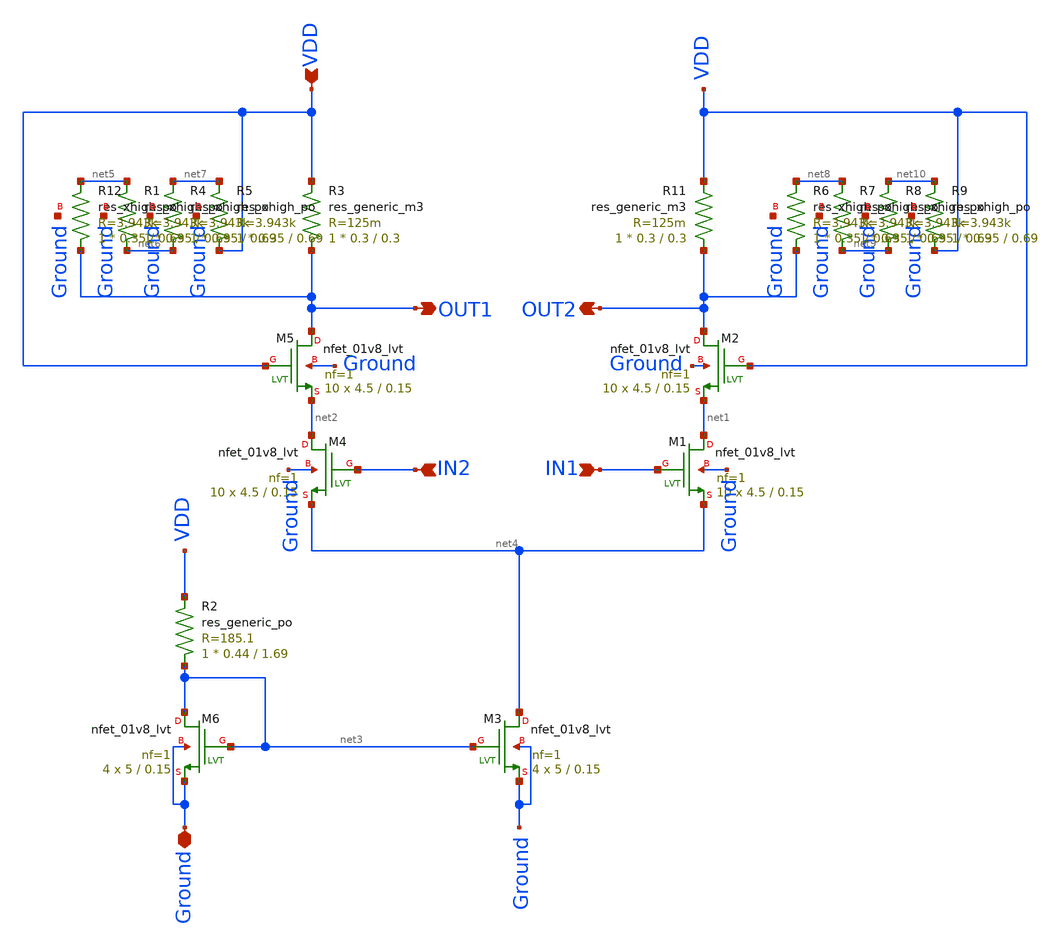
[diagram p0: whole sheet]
** sch_path: skywater_stuff/ECE631_RF_CMOS/Diff_LNA_LVS_1.sch
**.subckt Diff_LNA_LVS_1 IN1 IN2 VDD OUT1 OUT2 Ground
*.ipin IN1
*.ipin IN2
*.ipin VDD
*.opin OUT1
*.opin OUT2
*.iopin Ground
XM5 OUT1 VDD net2 Ground sky130_fd_pr__nfet_01v8_lvt L=0.15 W=4.5 nf=1 ad='int((nf+1)/2) * W/nf * 0.29'
+ as='int((nf+2)/2) * W/nf * 0.29' pd='2*int((nf+1)/2) * (W/nf + 0.29)' ps='2*int((nf+2)/2) * (W/nf + 0.29)'
+ nrd='0.29 / W' nrs='0.29 / W' sa=0 sb=0 sd=0 mult=10 m=10
XM3 net4 net3 Ground Ground sky130_fd_pr__nfet_01v8_lvt L=0.15 W=5 nf=1 ad='int((nf+1)/2) * W/nf * 0.29'
+ as='int((nf+2)/2) * W/nf * 0.29' pd='2*int((nf+1)/2) * (W/nf + 0.29)' ps='2*int((nf+2)/2) * (W/nf + 0.29)'
+ nrd='0.29 / W' nrs='0.29 / W' sa=0 sb=0 sd=0 mult=4 m=4
XM6 net3 net3 Ground Ground sky130_fd_pr__nfet_01v8_lvt L=0.15 W=5 nf=1 ad='int((nf+1)/2) * W/nf * 0.29'
+ as='int((nf+2)/2) * W/nf * 0.29' pd='2*int((nf+1)/2) * (W/nf + 0.29)' ps='2*int((nf+2)/2) * (W/nf + 0.29)'
+ nrd='0.29 / W' nrs='0.29 / W' sa=0 sb=0 sd=0 mult=4 m=4
XM4 net2 IN2 net4 Ground sky130_fd_pr__nfet_01v8_lvt L=0.15 W=4.5 nf=1 ad='int((nf+1)/2) * W/nf * 0.29'
+ as='int((nf+2)/2) * W/nf * 0.29' pd='2*int((nf+1)/2) * (W/nf + 0.29)' ps='2*int((nf+2)/2) * (W/nf + 0.29)'
+ nrd='0.29 / W' nrs='0.29 / W' sa=0 sb=0 sd=0 mult=10 m=10
XM2 OUT2 VDD net1 Ground sky130_fd_pr__nfet_01v8_lvt L=0.15 W=4.5 nf=1 ad='int((nf+1)/2) * W/nf * 0.29'
+ as='int((nf+2)/2) * W/nf * 0.29' pd='2*int((nf+1)/2) * (W/nf + 0.29)' ps='2*int((nf+2)/2) * (W/nf + 0.29)'
+ nrd='0.29 / W' nrs='0.29 / W' sa=0 sb=0 sd=0 mult=10 m=10
XM1 net1 IN1 net4 Ground sky130_fd_pr__nfet_01v8_lvt L=0.15 W=4.5 nf=1 ad='int((nf+1)/2) * W/nf * 0.29'
+ as='int((nf+2)/2) * W/nf * 0.29' pd='2*int((nf+1)/2) * (W/nf + 0.29)' ps='2*int((nf+2)/2) * (W/nf + 0.29)'
+ nrd='0.29 / W' nrs='0.29 / W' sa=0 sb=0 sd=0 mult=10 m=10
XR2 net3 VDD sky130_fd_pr__res_generic_po W=0.44 L=1.69 m=1
R3 OUT1 VDD sky130_fd_pr__res_generic_m3 W=0.3 L=0.3 m=1
R11 OUT2 VDD sky130_fd_pr__res_generic_m3 W=0.3 L=0.3 m=1
XR12 OUT1 net5 Ground sky130_fd_pr__res_xhigh_po W=0.35 L=0.69 mult=1 m=1
XR1 net6 net5 Ground sky130_fd_pr__res_xhigh_po W=0.35 L=0.69 mult=1 m=1
XR4 net6 net7 Ground sky130_fd_pr__res_xhigh_po W=0.35 L=0.69 mult=1 m=1
XR5 VDD net7 Ground sky130_fd_pr__res_xhigh_po W=0.35 L=0.69 mult=1 m=1
XR6 OUT2 net8 Ground sky130_fd_pr__res_xhigh_po W=0.35 L=0.69 mult=1 m=1
XR7 net9 net8 Ground sky130_fd_pr__res_xhigh_po W=0.35 L=0.69 mult=1 m=1
XR8 net9 net10 Ground sky130_fd_pr__res_xhigh_po W=0.35 L=0.69 mult=1 m=1
XR9 VDD net10 Ground sky130_fd_pr__res_xhigh_po W=0.35 L=0.69 mult=1 m=1
**.ends
.end
